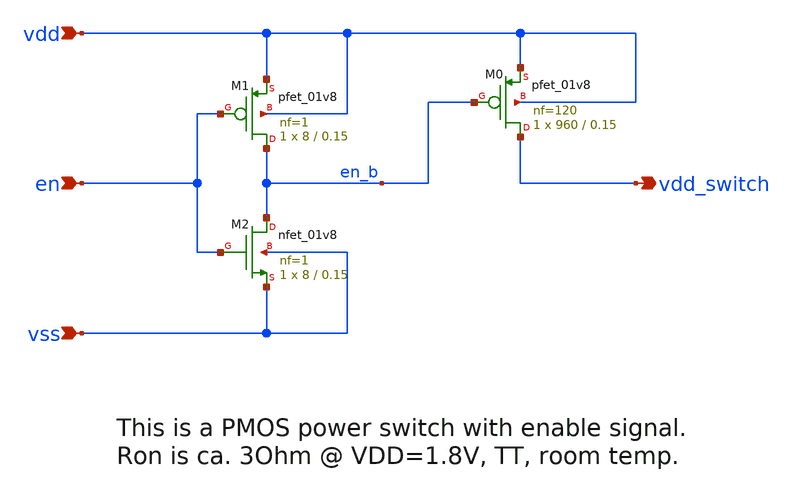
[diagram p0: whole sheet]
** sch_path: power_gate.sch
**.subckt power_gate en vdd_switch vdd vss
*.ipin en
*.opin vdd_switch
*.ipin vdd
*.ipin vss
XM0 vdd_switch en_b vdd vdd sky130_fd_pr__pfet_01v8 L=0.15 W=960 nf=120 ad='int((nf+1)/2) * W/nf * 0.29'
+ as='int((nf+2)/2) * W/nf * 0.29' pd='2*int((nf+1)/2) * (W/nf + 0.29)' ps='2*int((nf+2)/2) * (W/nf + 0.29)'
+ nrd='0.29 / W' nrs='0.29 / W' sa=0 sb=0 sd=0 mult=1 m=1
XM1 en_b en vdd vdd sky130_fd_pr__pfet_01v8 L=0.15 W=8 nf=1 ad='int((nf+1)/2) * W/nf * 0.29' as='int((nf+2)/2) * W/nf * 0.29'
+ pd='2*int((nf+1)/2) * (W/nf + 0.29)' ps='2*int((nf+2)/2) * (W/nf + 0.29)' nrd='0.29 / W' nrs='0.29 / W'
+ sa=0 sb=0 sd=0 mult=1 m=1
XM2 en_b en vss vss sky130_fd_pr__nfet_01v8 L=0.15 W=8 nf=1 ad='int((nf+1)/2) * W/nf * 0.29' as='int((nf+2)/2) * W/nf * 0.29'
+ pd='2*int((nf+1)/2) * (W/nf + 0.29)' ps='2*int((nf+2)/2) * (W/nf + 0.29)' nrd='0.29 / W' nrs='0.29 / W'
+ sa=0 sb=0 sd=0 mult=1 m=1
**.ends
.end
